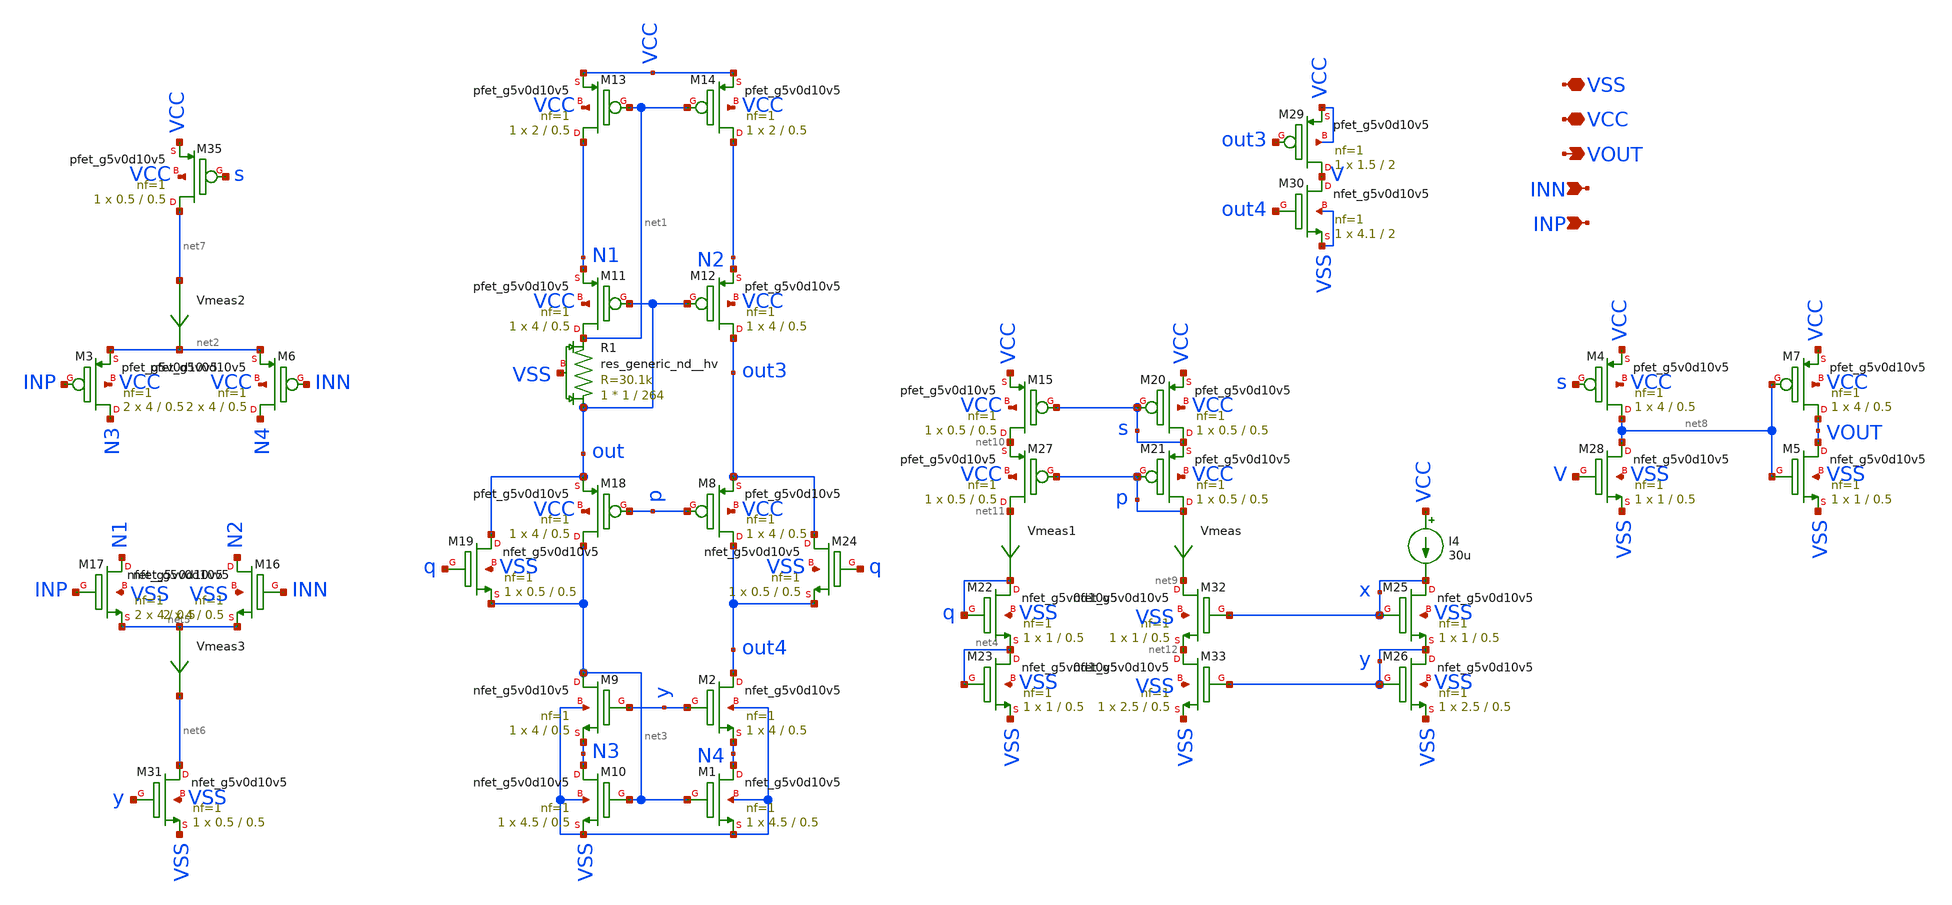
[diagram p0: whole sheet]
** sch_path: cadence_optimized/folded_cascode_ab.sch
**.subckt folded_cascode_ab VCC VOUT INN INP VSS
*.iopin VCC
*.opin VOUT
*.ipin INN
*.ipin INP
*.iopin VSS
XM1 N4 net3 VSS VSS sky130_fd_pr__nfet_g5v0d10v5 L=0.5 W=4.5 nf=1 ad='int((nf+1)/2) * W/nf * 0.29' as='int((nf+2)/2) * W/nf * 0.29'
+ pd='2*int((nf+1)/2) * (W/nf + 0.29)' ps='2*int((nf+2)/2) * (W/nf + 0.29)' nrd='0.29 / W' nrs='0.29 / W'
+ sa=0 sb=0 sd=0 mult=1 m=1
XM2 out4 y N4 VSS sky130_fd_pr__nfet_g5v0d10v5 L=0.5 W=4 nf=1 ad='int((nf+1)/2) * W/nf * 0.29' as='int((nf+2)/2) * W/nf * 0.29'
+ pd='2*int((nf+1)/2) * (W/nf + 0.29)' ps='2*int((nf+2)/2) * (W/nf + 0.29)' nrd='0.29 / W' nrs='0.29 / W'
+ sa=0 sb=0 sd=0 mult=1 m=1
XM9 net3 y N3 VSS sky130_fd_pr__nfet_g5v0d10v5 L=0.5 W=4 nf=1 ad='int((nf+1)/2) * W/nf * 0.29' as='int((nf+2)/2) * W/nf * 0.29'
+ pd='2*int((nf+1)/2) * (W/nf + 0.29)' ps='2*int((nf+2)/2) * (W/nf + 0.29)' nrd='0.29 / W' nrs='0.29 / W'
+ sa=0 sb=0 sd=0 mult=1 m=1
XM10 N3 net3 VSS VSS sky130_fd_pr__nfet_g5v0d10v5 L=0.5 W=4.5 nf=1 ad='int((nf+1)/2) * W/nf * 0.29' as='int((nf+2)/2) * W/nf * 0.29'
+ pd='2*int((nf+1)/2) * (W/nf + 0.29)' ps='2*int((nf+2)/2) * (W/nf + 0.29)' nrd='0.29 / W' nrs='0.29 / W'
+ sa=0 sb=0 sd=0 mult=1 m=1
XM11 net1 out N1 VCC sky130_fd_pr__pfet_g5v0d10v5 L=0.5 W=4 nf=1 ad='int((nf+1)/2) * W/nf * 0.29' as='int((nf+2)/2) * W/nf * 0.29'
+ pd='2*int((nf+1)/2) * (W/nf + 0.29)' ps='2*int((nf+2)/2) * (W/nf + 0.29)' nrd='0.29 / W' nrs='0.29 / W'
+ sa=0 sb=0 sd=0 mult=1 m=1
XM12 out3 out N2 VCC sky130_fd_pr__pfet_g5v0d10v5 L=0.5 W=4 nf=1 ad='int((nf+1)/2) * W/nf * 0.29' as='int((nf+2)/2) * W/nf * 0.29'
+ pd='2*int((nf+1)/2) * (W/nf + 0.29)' ps='2*int((nf+2)/2) * (W/nf + 0.29)' nrd='0.29 / W' nrs='0.29 / W'
+ sa=0 sb=0 sd=0 mult=1 m=1
XM13 N1 net1 VCC VCC sky130_fd_pr__pfet_g5v0d10v5 L=0.5 W=2 nf=1 ad='int((nf+1)/2) * W/nf * 0.29' as='int((nf+2)/2) * W/nf * 0.29'
+ pd='2*int((nf+1)/2) * (W/nf + 0.29)' ps='2*int((nf+2)/2) * (W/nf + 0.29)' nrd='0.29 / W' nrs='0.29 / W'
+ sa=0 sb=0 sd=0 mult=1 m=1
XM14 N2 net1 VCC VCC sky130_fd_pr__pfet_g5v0d10v5 L=0.5 W=2 nf=1 ad='int((nf+1)/2) * W/nf * 0.29' as='int((nf+2)/2) * W/nf * 0.29'
+ pd='2*int((nf+1)/2) * (W/nf + 0.29)' ps='2*int((nf+2)/2) * (W/nf + 0.29)' nrd='0.29 / W' nrs='0.29 / W'
+ sa=0 sb=0 sd=0 mult=1 m=1
XM16 N2 INN net5 VSS sky130_fd_pr__nfet_g5v0d10v5 L=0.5 W=4 nf=1 ad='int((nf+1)/2) * W/nf * 0.29' as='int((nf+2)/2) * W/nf * 0.29'
+ pd='2*int((nf+1)/2) * (W/nf + 0.29)' ps='2*int((nf+2)/2) * (W/nf + 0.29)' nrd='0.29 / W' nrs='0.29 / W'
+ sa=0 sb=0 sd=0 mult=2 m=2
XM6 N4 INN net2 VCC sky130_fd_pr__pfet_g5v0d10v5 L=0.5 W=4 nf=1 ad='int((nf+1)/2) * W/nf * 0.29' as='int((nf+2)/2) * W/nf * 0.29'
+ pd='2*int((nf+1)/2) * (W/nf + 0.29)' ps='2*int((nf+2)/2) * (W/nf + 0.29)' nrd='0.29 / W' nrs='0.29 / W'
+ sa=0 sb=0 sd=0 mult=2 m=2
Vmeas2 net7 net2 0
.save i(vmeas2)
XM20 s s VCC VCC sky130_fd_pr__pfet_g5v0d10v5 L=0.5 W=0.5 nf=1 ad='int((nf+1)/2) * W/nf * 0.29' as='int((nf+2)/2) * W/nf * 0.29'
+ pd='2*int((nf+1)/2) * (W/nf + 0.29)' ps='2*int((nf+2)/2) * (W/nf + 0.29)' nrd='0.29 / W' nrs='0.29 / W'
+ sa=0 sb=0 sd=0 mult=1 m=1
XM21 p p s VCC sky130_fd_pr__pfet_g5v0d10v5 L=0.5 W=0.5 nf=1 ad='int((nf+1)/2) * W/nf * 0.29' as='int((nf+2)/2) * W/nf * 0.29'
+ pd='2*int((nf+1)/2) * (W/nf + 0.29)' ps='2*int((nf+2)/2) * (W/nf + 0.29)' nrd='0.29 / W' nrs='0.29 / W'
+ sa=0 sb=0 sd=0 mult=1 m=1
XM22 q q net4 VSS sky130_fd_pr__nfet_g5v0d10v5 L=0.5 W=1 nf=1 ad='int((nf+1)/2) * W/nf * 0.29' as='int((nf+2)/2) * W/nf * 0.29'
+ pd='2*int((nf+1)/2) * (W/nf + 0.29)' ps='2*int((nf+2)/2) * (W/nf + 0.29)' nrd='0.29 / W' nrs='0.29 / W'
+ sa=0 sb=0 sd=0 mult=1 m=1
XM23 net4 net4 VSS VSS sky130_fd_pr__nfet_g5v0d10v5 L=0.5 W=1 nf=1 ad='int((nf+1)/2) * W/nf * 0.29' as='int((nf+2)/2) * W/nf * 0.29'
+ pd='2*int((nf+1)/2) * (W/nf + 0.29)' ps='2*int((nf+2)/2) * (W/nf + 0.29)' nrd='0.29 / W' nrs='0.29 / W'
+ sa=0 sb=0 sd=0 mult=1 m=1
XM29 V out3 VCC VCC sky130_fd_pr__pfet_g5v0d10v5 L=2 W=1.5 nf=1 ad='int((nf+1)/2) * W/nf * 0.29' as='int((nf+2)/2) * W/nf * 0.29'
+ pd='2*int((nf+1)/2) * (W/nf + 0.29)' ps='2*int((nf+2)/2) * (W/nf + 0.29)' nrd='0.29 / W' nrs='0.29 / W'
+ sa=0 sb=0 sd=0 mult=1 m=1
XM30 V out4 VSS VSS sky130_fd_pr__nfet_g5v0d10v5 L=2 W=4.1 nf=1 ad='int((nf+1)/2) * W/nf * 0.29' as='int((nf+2)/2) * W/nf * 0.29'
+ pd='2*int((nf+1)/2) * (W/nf + 0.29)' ps='2*int((nf+2)/2) * (W/nf + 0.29)' nrd='0.29 / W' nrs='0.29 / W'
+ sa=0 sb=0 sd=0 mult=1 m=1
XM17 N1 INP net5 VSS sky130_fd_pr__nfet_g5v0d10v5 L=0.5 W=4 nf=1 ad='int((nf+1)/2) * W/nf * 0.29' as='int((nf+2)/2) * W/nf * 0.29'
+ pd='2*int((nf+1)/2) * (W/nf + 0.29)' ps='2*int((nf+2)/2) * (W/nf + 0.29)' nrd='0.29 / W' nrs='0.29 / W'
+ sa=0 sb=0 sd=0 mult=2 m=2
XM3 N3 INP net2 VCC sky130_fd_pr__pfet_g5v0d10v5 L=0.5 W=4 nf=1 ad='int((nf+1)/2) * W/nf * 0.29' as='int((nf+2)/2) * W/nf * 0.29'
+ pd='2*int((nf+1)/2) * (W/nf + 0.29)' ps='2*int((nf+2)/2) * (W/nf + 0.29)' nrd='0.29 / W' nrs='0.29 / W'
+ sa=0 sb=0 sd=0 mult=2 m=2
XM8 out4 p out3 VCC sky130_fd_pr__pfet_g5v0d10v5 L=0.5 W=4 nf=1 ad='int((nf+1)/2) * W/nf * 0.29' as='int((nf+2)/2) * W/nf * 0.29'
+ pd='2*int((nf+1)/2) * (W/nf + 0.29)' ps='2*int((nf+2)/2) * (W/nf + 0.29)' nrd='0.29 / W' nrs='0.29 / W'
+ sa=0 sb=0 sd=0 mult=1 m=1
XM18 net3 p out VCC sky130_fd_pr__pfet_g5v0d10v5 L=0.5 W=4 nf=1 ad='int((nf+1)/2) * W/nf * 0.29' as='int((nf+2)/2) * W/nf * 0.29'
+ pd='2*int((nf+1)/2) * (W/nf + 0.29)' ps='2*int((nf+2)/2) * (W/nf + 0.29)' nrd='0.29 / W' nrs='0.29 / W'
+ sa=0 sb=0 sd=0 mult=1 m=1
XM19 out q net3 VSS sky130_fd_pr__nfet_g5v0d10v5 L=0.5 W=0.5 nf=1 ad='int((nf+1)/2) * W/nf * 0.29' as='int((nf+2)/2) * W/nf * 0.29'
+ pd='2*int((nf+1)/2) * (W/nf + 0.29)' ps='2*int((nf+2)/2) * (W/nf + 0.29)' nrd='0.29 / W' nrs='0.29 / W'
+ sa=0 sb=0 sd=0 mult=1 m=1
XM24 out3 q out4 VSS sky130_fd_pr__nfet_g5v0d10v5 L=0.5 W=0.5 nf=1 ad='int((nf+1)/2) * W/nf * 0.29' as='int((nf+2)/2) * W/nf * 0.29'
+ pd='2*int((nf+1)/2) * (W/nf + 0.29)' ps='2*int((nf+2)/2) * (W/nf + 0.29)' nrd='0.29 / W' nrs='0.29 / W'
+ sa=0 sb=0 sd=0 mult=1 m=1
Vmeas p net9 0
.save i(vmeas)
XM25 x x y VSS sky130_fd_pr__nfet_g5v0d10v5 L=0.5 W=1 nf=1 ad='int((nf+1)/2) * W/nf * 0.29' as='int((nf+2)/2) * W/nf * 0.29'
+ pd='2*int((nf+1)/2) * (W/nf + 0.29)' ps='2*int((nf+2)/2) * (W/nf + 0.29)' nrd='0.29 / W' nrs='0.29 / W'
+ sa=0 sb=0 sd=0 mult=1 m=1
XM26 y y VSS VSS sky130_fd_pr__nfet_g5v0d10v5 L=0.5 W=2.5 nf=1 ad='int((nf+1)/2) * W/nf * 0.29' as='int((nf+2)/2) * W/nf * 0.29'
+ pd='2*int((nf+1)/2) * (W/nf + 0.29)' ps='2*int((nf+2)/2) * (W/nf + 0.29)' nrd='0.29 / W' nrs='0.29 / W'
+ sa=0 sb=0 sd=0 mult=1 m=1
I4 VCC x 30u
XM15 net10 s VCC VCC sky130_fd_pr__pfet_g5v0d10v5 L=0.5 W=0.5 nf=1 ad='int((nf+1)/2) * W/nf * 0.29' as='int((nf+2)/2) * W/nf * 0.29'
+ pd='2*int((nf+1)/2) * (W/nf + 0.29)' ps='2*int((nf+2)/2) * (W/nf + 0.29)' nrd='0.29 / W' nrs='0.29 / W'
+ sa=0 sb=0 sd=0 mult=1 m=1
XM27 net11 p net10 VCC sky130_fd_pr__pfet_g5v0d10v5 L=0.5 W=0.5 nf=1 ad='int((nf+1)/2) * W/nf * 0.29'
+ as='int((nf+2)/2) * W/nf * 0.29' pd='2*int((nf+1)/2) * (W/nf + 0.29)' ps='2*int((nf+2)/2) * (W/nf + 0.29)'
+ nrd='0.29 / W' nrs='0.29 / W' sa=0 sb=0 sd=0 mult=1 m=1
Vmeas1 net11 q 0
.save i(vmeas1)
XM31 net6 y VSS VSS sky130_fd_pr__nfet_g5v0d10v5 L=0.5 W=0.5 nf=1 ad='int((nf+1)/2) * W/nf * 0.29' as='int((nf+2)/2) * W/nf * 0.29'
+ pd='2*int((nf+1)/2) * (W/nf + 0.29)' ps='2*int((nf+2)/2) * (W/nf + 0.29)' nrd='0.29 / W' nrs='0.29 / W'
+ sa=0 sb=0 sd=0 mult=1 m=1
Vmeas3 net5 net6 0
.save i(vmeas3)
XM35 net7 s VCC VCC sky130_fd_pr__pfet_g5v0d10v5 L=0.5 W=0.5 nf=1 ad='int((nf+1)/2) * W/nf * 0.29' as='int((nf+2)/2) * W/nf * 0.29'
+ pd='2*int((nf+1)/2) * (W/nf + 0.29)' ps='2*int((nf+2)/2) * (W/nf + 0.29)' nrd='0.29 / W' nrs='0.29 / W'
+ sa=0 sb=0 sd=0 mult=1 m=1
XR1 out net1 VSS sky130_fd_pr__res_generic_nd__hv W=1 L=264 mult=1 m=1
XM28 net8 V VSS VSS sky130_fd_pr__nfet_g5v0d10v5 L=0.5 W=1 nf=1 ad='int((nf+1)/2) * W/nf * 0.29' as='int((nf+2)/2) * W/nf * 0.29'
+ pd='2*int((nf+1)/2) * (W/nf + 0.29)' ps='2*int((nf+2)/2) * (W/nf + 0.29)' nrd='0.29 / W' nrs='0.29 / W'
+ sa=0 sb=0 sd=0 mult=1 m=1
XM4 net8 s VCC VCC sky130_fd_pr__pfet_g5v0d10v5 L=0.5 W=4 nf=1 ad='int((nf+1)/2) * W/nf * 0.29' as='int((nf+2)/2) * W/nf * 0.29'
+ pd='2*int((nf+1)/2) * (W/nf + 0.29)' ps='2*int((nf+2)/2) * (W/nf + 0.29)' nrd='0.29 / W' nrs='0.29 / W'
+ sa=0 sb=0 sd=0 mult=1 m=1
XM32 net9 x net12 VSS sky130_fd_pr__nfet_g5v0d10v5 L=0.5 W=1 nf=1 ad='int((nf+1)/2) * W/nf * 0.29' as='int((nf+2)/2) * W/nf * 0.29'
+ pd='2*int((nf+1)/2) * (W/nf + 0.29)' ps='2*int((nf+2)/2) * (W/nf + 0.29)' nrd='0.29 / W' nrs='0.29 / W'
+ sa=0 sb=0 sd=0 mult=1 m=1
XM33 net12 y VSS VSS sky130_fd_pr__nfet_g5v0d10v5 L=0.5 W=2.5 nf=1 ad='int((nf+1)/2) * W/nf * 0.29' as='int((nf+2)/2) * W/nf * 0.29'
+ pd='2*int((nf+1)/2) * (W/nf + 0.29)' ps='2*int((nf+2)/2) * (W/nf + 0.29)' nrd='0.29 / W' nrs='0.29 / W'
+ sa=0 sb=0 sd=0 mult=1 m=1
XM5 VOUT net8 VSS VSS sky130_fd_pr__nfet_g5v0d10v5 L=0.5 W=1 nf=1 ad='int((nf+1)/2) * W/nf * 0.29' as='int((nf+2)/2) * W/nf * 0.29'
+ pd='2*int((nf+1)/2) * (W/nf + 0.29)' ps='2*int((nf+2)/2) * (W/nf + 0.29)' nrd='0.29 / W' nrs='0.29 / W'
+ sa=0 sb=0 sd=0 mult=1 m=1
XM7 VOUT net8 VCC VCC sky130_fd_pr__pfet_g5v0d10v5 L=0.5 W=4 nf=1 ad='int((nf+1)/2) * W/nf * 0.29' as='int((nf+2)/2) * W/nf * 0.29'
+ pd='2*int((nf+1)/2) * (W/nf + 0.29)' ps='2*int((nf+2)/2) * (W/nf + 0.29)' nrd='0.29 / W' nrs='0.29 / W'
+ sa=0 sb=0 sd=0 mult=1 m=1
**.ends
.end
